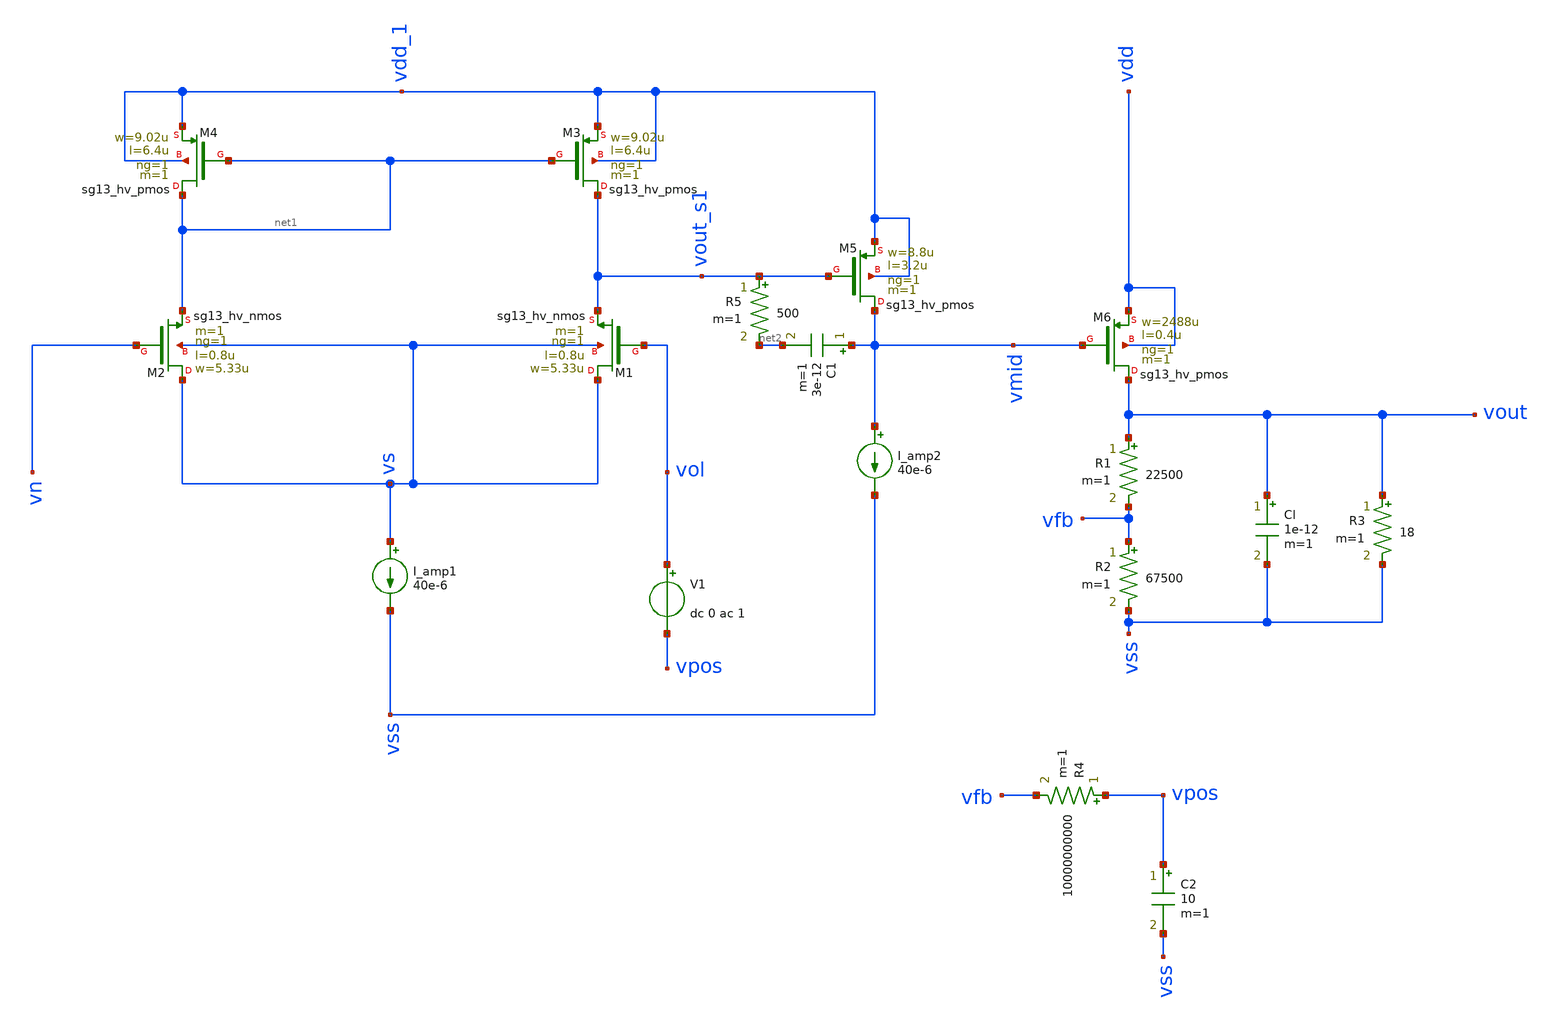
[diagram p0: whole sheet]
** sch_path: test/Tesis_notebooks/xschem/ldo_ol_tb.sch
**.subckt ldo_ol_tb
I_amp1 vs vss 40e-6
I_amp2 vmid vss 40e-6
R1 vout vfb 22500 m=1
R2 vfb vss 67500 m=1
Cl vout vss 1e-12 m=1
XM1 vs vol vout_s1 vs sg13_hv_nmos w=5.33u l=0.8u ng=1 m=1 mm_ok=1
XM2 vs vn net1 vs sg13_hv_nmos w=5.33u l=0.8u ng=1 m=1 mm_ok=1
XM3 vout_s1 net1 vdd_1 vdd_1 sg13_hv_pmos w=9.02u l=6.4u ng=1 m=1 mm_ok=1
XM4 net1 net1 vdd_1 vdd_1 sg13_hv_pmos w=9.02u l=6.4u ng=1 m=1 mm_ok=1
XM5 vmid vout_s1 vdd_1 vdd_1 sg13_hv_pmos w=8.8u l=3.2u ng=1 m=1 mm_ok=1
XM6 vout vmid vdd vdd sg13_hv_pmos w=2488u l=0.4u ng=1 m=1 mm_ok=1
R4 vpos vfb 10000000000 m=1
C2 vpos vss 10 m=1
V1 vol vpos dc 0 ac 1
R3 vout vss 18 m=1
R5 vout_s1 net2 500 m=1
C1 vmid net2 3e-12 m=1
**** begin user architecture code



.lib /opt/pdks/ihp-sg13g2/libs.tech/ngspice/models/cornerMOShv.lib mos_tt

Vref vn 0 1.35
Vdd vdd 0 3.3
Vdd_1 vdd_1 0 3.3
Vss vss 0 0

.control
ac dec 10 1 100G
plot vdb(vout)
plot phase(vout)
op
print vout vmid vout_s1 vs

let gm_m1 = @n.xm1.nsg13_hv_nmos[gm]
let gm_m2 = @n.xm2.nsg13_hv_nmos[gm]
let gm_m3 = @n.xm3.nsg13_hv_pmos[gm]
let gm_m4 = @n.xm4.nsg13_hv_pmos[gm]
let gm_m5 = @n.xm5.nsg13_hv_pmos[gm]
let gm_m6 = @n.xm6.nsg13_hv_pmos[gm]

let gds_m1 = @n.xm1.nsg13_hv_nmos[gds]
let gds_m2 = @n.xm2.nsg13_hv_nmos[gds]
let gds_m3 = @n.xm3.nsg13_hv_pmos[gds]
let gds_m4 = @n.xm4.nsg13_hv_pmos[gds]
let gds_m5 = @n.xm5.nsg13_hv_pmos[gds]
let gds_m6 = @n.xm6.nsg13_hv_pmos[gds]

print gm_m1
print gm_m2
print gm_m3
print gm_m4
print gm_m5
print gm_m6

print 1/gds_m1
print 1/gds_m2
print 1/gds_m3
print 1/gds_m4
print 1/gds_m5
print 1/gds_m6

.endc



**** end user architecture code
**.ends
.end
